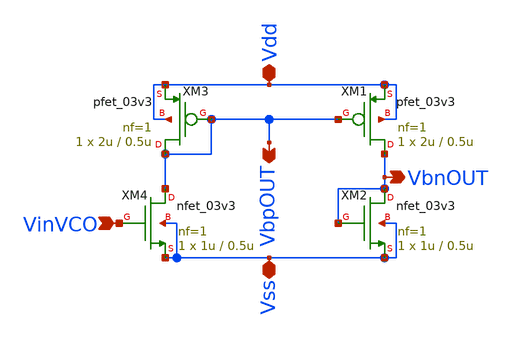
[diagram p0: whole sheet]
** sch_path: src/analog/biasing.sch
**.subckt biasing Vdd Vss VinVCO VbpOUT VbnOUT
*.iopin Vdd
*.iopin Vss
*.ipin VinVCO
*.opin VbpOUT
*.opin VbnOUT
XM3 VbpOUT VbpOUT Vdd Vdd pfet_03v3 L=0.5u W=2u nf=1 ad='int((nf+1)/2) * W/nf * 0.18u' as='int((nf+2)/2) * W/nf * 0.18u'
+ pd='2*int((nf+1)/2) * (W/nf + 0.18u)' ps='2*int((nf+2)/2) * (W/nf + 0.18u)' nrd='0.18u / W' nrs='0.18u / W'
+ sa=0 sb=0 sd=0 m=1
XM4 VbpOUT VinVCO Vss Vss nfet_03v3 L=0.5u W=1u nf=1 ad='int((nf+1)/2) * W/nf * 0.18u' as='int((nf+2)/2) * W/nf * 0.18u'
+ pd='2*int((nf+1)/2) * (W/nf + 0.18u)' ps='2*int((nf+2)/2) * (W/nf + 0.18u)' nrd='0.18u / W' nrs='0.18u / W'
+ sa=0 sb=0 sd=0 m=1
XM1 VbnOUT VbpOUT Vdd Vdd pfet_03v3 L=0.5u W=2u nf=1 ad='int((nf+1)/2) * W/nf * 0.18u' as='int((nf+2)/2) * W/nf * 0.18u'
+ pd='2*int((nf+1)/2) * (W/nf + 0.18u)' ps='2*int((nf+2)/2) * (W/nf + 0.18u)' nrd='0.18u / W' nrs='0.18u / W'
+ sa=0 sb=0 sd=0 m=1
XM2 VbnOUT VbnOUT Vss Vss nfet_03v3 L=0.5u W=1u nf=1 ad='int((nf+1)/2) * W/nf * 0.18u' as='int((nf+2)/2) * W/nf * 0.18u'
+ pd='2*int((nf+1)/2) * (W/nf + 0.18u)' ps='2*int((nf+2)/2) * (W/nf + 0.18u)' nrd='0.18u / W' nrs='0.18u / W'
+ sa=0 sb=0 sd=0 m=1
**.ends
.end
